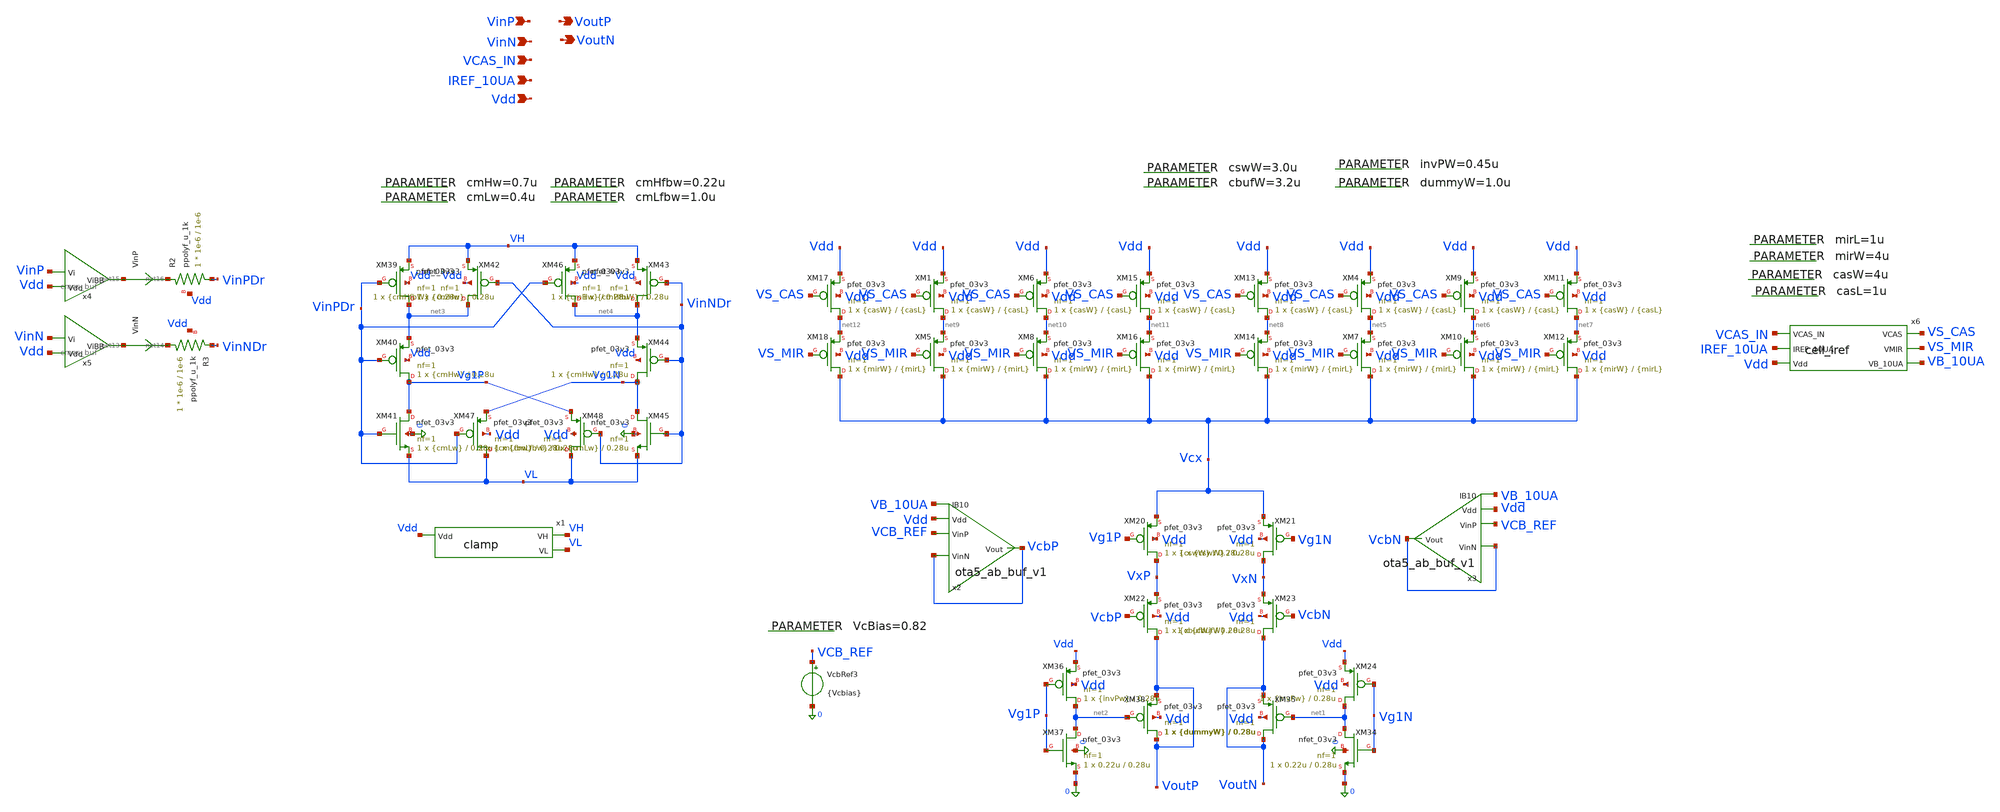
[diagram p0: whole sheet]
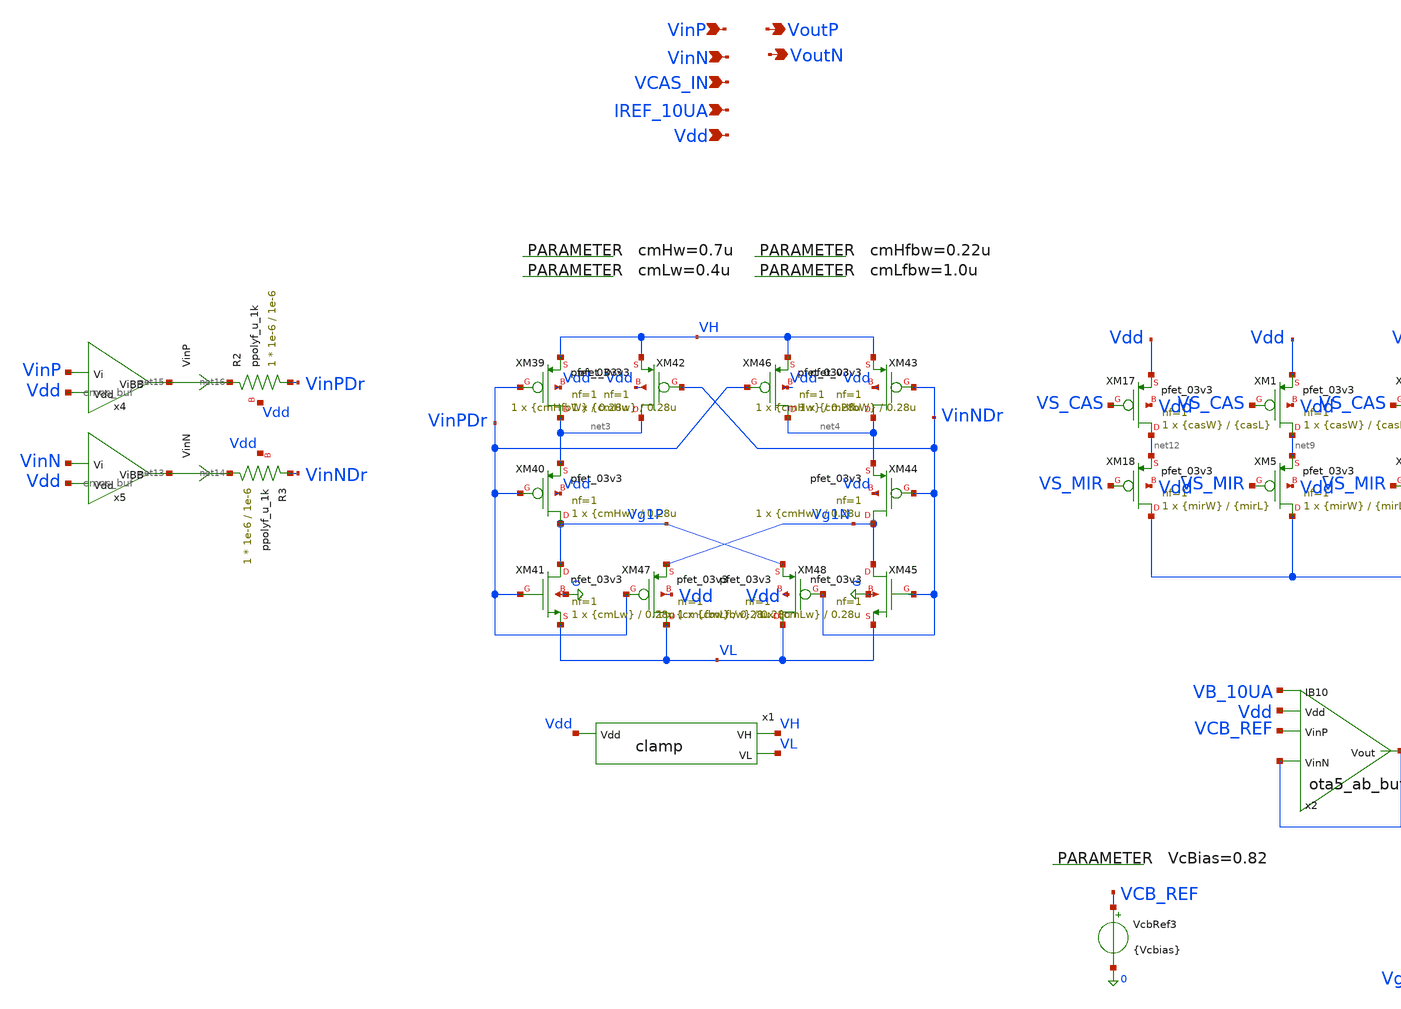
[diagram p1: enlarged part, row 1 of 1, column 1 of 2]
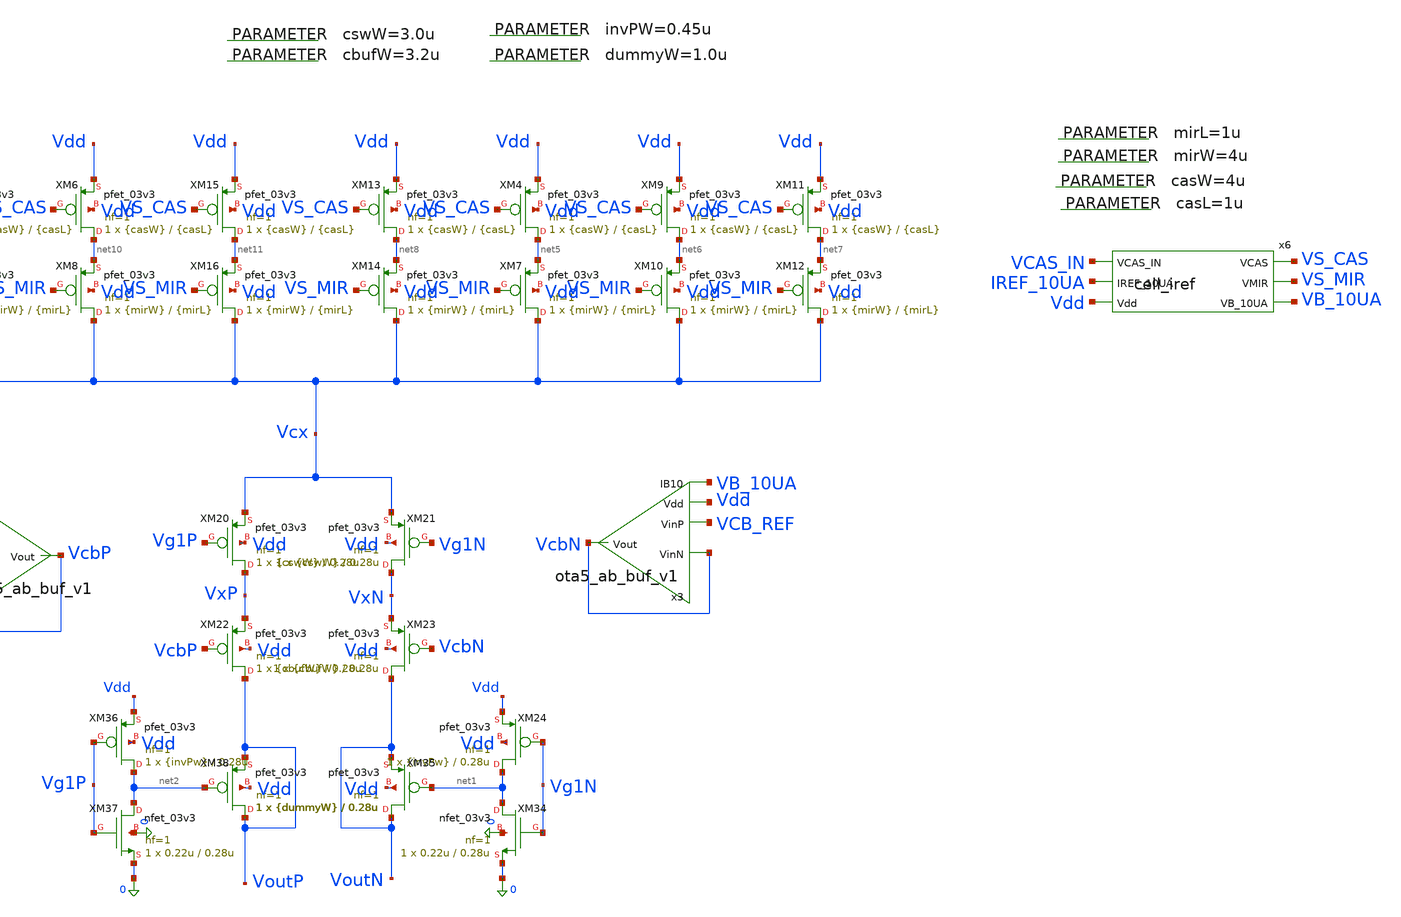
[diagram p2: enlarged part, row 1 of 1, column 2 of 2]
** sch_path: blocks/dac/cellv9/dac_cell_80ua_v9.sch
**.subckt dac_cell_80ua_v9 VoutP VoutN VinP VinN Vdd VCAS_IN IREF_10UA
*.opin VoutP
*.opin VoutN
*.ipin VinP
*.ipin VinN
*.ipin Vdd
*.ipin VCAS_IN
*.ipin IREF_10UA
.param cmLw=0.4u
.param cmHw=0.7u
.param cmLfbw=1.0u
.param cmHfbw=0.22u
XM20 VxP Vg1P Vcx Vdd pfet_03v3 L=0.28u W={cswW} nf=1 ad='int((nf+1)/2) * W/nf * 0.18u' as='int((nf+2)/2) * W/nf * 0.18u'
+ pd='2*int((nf+1)/2) * (W/nf + 0.18u)' ps='2*int((nf+2)/2) * (W/nf + 0.18u)' nrd='0.18u / W' nrs='0.18u / W'
+ sa=0 sb=0 sd=0 m=1
XM21 VxN Vg1N Vcx Vdd pfet_03v3 L=0.28u W={cswW} nf=1 ad='int((nf+1)/2) * W/nf * 0.18u' as='int((nf+2)/2) * W/nf * 0.18u'
+ pd='2*int((nf+1)/2) * (W/nf + 0.18u)' ps='2*int((nf+2)/2) * (W/nf + 0.18u)' nrd='0.18u / W' nrs='0.18u / W'
+ sa=0 sb=0 sd=0 m=1
XM22 VoutP VcbP VxP Vdd pfet_03v3 L=0.28u W={cbufW} nf=1 ad='int((nf+1)/2) * W/nf * 0.18u' as='int((nf+2)/2) * W/nf * 0.18u'
+ pd='2*int((nf+1)/2) * (W/nf + 0.18u)' ps='2*int((nf+2)/2) * (W/nf + 0.18u)' nrd='0.18u / W' nrs='0.18u / W'
+ sa=0 sb=0 sd=0 m=1
XM23 VoutN VcbN VxN Vdd pfet_03v3 L=0.28u W={cbufW} nf=1 ad='int((nf+1)/2) * W/nf * 0.18u' as='int((nf+2)/2) * W/nf * 0.18u'
+ pd='2*int((nf+1)/2) * (W/nf + 0.18u)' ps='2*int((nf+2)/2) * (W/nf + 0.18u)' nrd='0.18u / W' nrs='0.18u / W'
+ sa=0 sb=0 sd=0 m=1
XM24 net1 Vg1N Vdd Vdd pfet_03v3 L=0.28u W={invPw} nf=1 ad='int((nf+1)/2) * W/nf * 0.18u' as='int((nf+2)/2) * W/nf * 0.18u'
+ pd='2*int((nf+1)/2) * (W/nf + 0.18u)' ps='2*int((nf+2)/2) * (W/nf + 0.18u)' nrd='0.18u / W' nrs='0.18u / W'
+ sa=0 sb=0 sd=0 m=1
XM34 net1 Vg1N 0 0 nfet_03v3 L=0.28u W=0.22u nf=1 ad='int((nf+1)/2) * W/nf * 0.18u' as='int((nf+2)/2) * W/nf * 0.18u'
+ pd='2*int((nf+1)/2) * (W/nf + 0.18u)' ps='2*int((nf+2)/2) * (W/nf + 0.18u)' nrd='0.18u / W' nrs='0.18u / W'
+ sa=0 sb=0 sd=0 m=1
XM35 VoutN net1 VoutN Vdd pfet_03v3 L=0.28u W={dummyW} nf=1 ad='int((nf+1)/2) * W/nf * 0.18u' as='int((nf+2)/2) * W/nf * 0.18u'
+ pd='2*int((nf+1)/2) * (W/nf + 0.18u)' ps='2*int((nf+2)/2) * (W/nf + 0.18u)' nrd='0.18u / W' nrs='0.18u / W'
+ sa=0 sb=0 sd=0 m=1
XM36 net2 Vg1P Vdd Vdd pfet_03v3 L=0.28u W={invPw} nf=1 ad='int((nf+1)/2) * W/nf * 0.18u' as='int((nf+2)/2) * W/nf * 0.18u'
+ pd='2*int((nf+1)/2) * (W/nf + 0.18u)' ps='2*int((nf+2)/2) * (W/nf + 0.18u)' nrd='0.18u / W' nrs='0.18u / W'
+ sa=0 sb=0 sd=0 m=1
XM37 net2 Vg1P 0 0 nfet_03v3 L=0.28u W=0.22u nf=1 ad='int((nf+1)/2) * W/nf * 0.18u' as='int((nf+2)/2) * W/nf * 0.18u'
+ pd='2*int((nf+1)/2) * (W/nf + 0.18u)' ps='2*int((nf+2)/2) * (W/nf + 0.18u)' nrd='0.18u / W' nrs='0.18u / W'
+ sa=0 sb=0 sd=0 m=1
XM38 VoutP net2 VoutP Vdd pfet_03v3 L=0.28u W={dummyW} nf=1 ad='int((nf+1)/2) * W/nf * 0.18u' as='int((nf+2)/2) * W/nf * 0.18u'
+ pd='2*int((nf+1)/2) * (W/nf + 0.18u)' ps='2*int((nf+2)/2) * (W/nf + 0.18u)' nrd='0.18u / W' nrs='0.18u / W'
+ sa=0 sb=0 sd=0 m=1
VcbRef3 VCB_REF 0 {Vcbias}
.save i(vcbref3)
.param VcBias=0.82
XM39 net3 VinPDr VH Vdd pfet_03v3 L=0.28u W={cmHw} nf=1 ad='int((nf+1)/2) * W/nf * 0.18u' as='int((nf+2)/2) * W/nf * 0.18u'
+ pd='2*int((nf+1)/2) * (W/nf + 0.18u)' ps='2*int((nf+2)/2) * (W/nf + 0.18u)' nrd='0.18u / W' nrs='0.18u / W'
+ sa=0 sb=0 sd=0 m=1
XM40 Vg1P VinPDr net3 Vdd pfet_03v3 L=0.28u W={cmHw} nf=1 ad='int((nf+1)/2) * W/nf * 0.18u' as='int((nf+2)/2) * W/nf * 0.18u'
+ pd='2*int((nf+1)/2) * (W/nf + 0.18u)' ps='2*int((nf+2)/2) * (W/nf + 0.18u)' nrd='0.18u / W' nrs='0.18u / W'
+ sa=0 sb=0 sd=0 m=1
XM41 Vg1P VinPDr VL 0 nfet_03v3 L=0.28u W={cmLw} nf=1 ad='int((nf+1)/2) * W/nf * 0.18u' as='int((nf+2)/2) * W/nf * 0.18u'
+ pd='2*int((nf+1)/2) * (W/nf + 0.18u)' ps='2*int((nf+2)/2) * (W/nf + 0.18u)' nrd='0.18u / W' nrs='0.18u / W'
+ sa=0 sb=0 sd=0 m=1
XM42 net3 VinNDr VH Vdd pfet_03v3 L=0.28u W={cmHfbW} nf=1 ad='int((nf+1)/2) * W/nf * 0.18u' as='int((nf+2)/2) * W/nf * 0.18u'
+ pd='2*int((nf+1)/2) * (W/nf + 0.18u)' ps='2*int((nf+2)/2) * (W/nf + 0.18u)' nrd='0.18u / W' nrs='0.18u / W'
+ sa=0 sb=0 sd=0 m=1
XM43 net4 VinNDr VH Vdd pfet_03v3 L=0.28u W={cmHw} nf=1 ad='int((nf+1)/2) * W/nf * 0.18u' as='int((nf+2)/2) * W/nf * 0.18u'
+ pd='2*int((nf+1)/2) * (W/nf + 0.18u)' ps='2*int((nf+2)/2) * (W/nf + 0.18u)' nrd='0.18u / W' nrs='0.18u / W'
+ sa=0 sb=0 sd=0 m=1
XM44 Vg1N VinNDr net4 Vdd pfet_03v3 L=0.28u W={cmHw} nf=1 ad='int((nf+1)/2) * W/nf * 0.18u' as='int((nf+2)/2) * W/nf * 0.18u'
+ pd='2*int((nf+1)/2) * (W/nf + 0.18u)' ps='2*int((nf+2)/2) * (W/nf + 0.18u)' nrd='0.18u / W' nrs='0.18u / W'
+ sa=0 sb=0 sd=0 m=1
XM45 Vg1N VinNDr VL 0 nfet_03v3 L=0.28u W={cmLw} nf=1 ad='int((nf+1)/2) * W/nf * 0.18u' as='int((nf+2)/2) * W/nf * 0.18u'
+ pd='2*int((nf+1)/2) * (W/nf + 0.18u)' ps='2*int((nf+2)/2) * (W/nf + 0.18u)' nrd='0.18u / W' nrs='0.18u / W'
+ sa=0 sb=0 sd=0 m=1
XM46 net4 VinPDr VH Vdd pfet_03v3 L=0.28u W={cmHfbW} nf=1 ad='int((nf+1)/2) * W/nf * 0.18u' as='int((nf+2)/2) * W/nf * 0.18u'
+ pd='2*int((nf+1)/2) * (W/nf + 0.18u)' ps='2*int((nf+2)/2) * (W/nf + 0.18u)' nrd='0.18u / W' nrs='0.18u / W'
+ sa=0 sb=0 sd=0 m=1
XM47 VL VinPDr Vg1N Vdd pfet_03v3 L=0.28u W={cmLfbw} nf=1 ad='int((nf+1)/2) * W/nf * 0.18u' as='int((nf+2)/2) * W/nf * 0.18u'
+ pd='2*int((nf+1)/2) * (W/nf + 0.18u)' ps='2*int((nf+2)/2) * (W/nf + 0.18u)' nrd='0.18u / W' nrs='0.18u / W'
+ sa=0 sb=0 sd=0 m=1
XM48 VL VinNDr Vg1P Vdd pfet_03v3 L=0.28u W={cmLfbw} nf=1 ad='int((nf+1)/2) * W/nf * 0.18u' as='int((nf+2)/2) * W/nf * 0.18u'
+ pd='2*int((nf+1)/2) * (W/nf + 0.18u)' ps='2*int((nf+2)/2) * (W/nf + 0.18u)' nrd='0.18u / W' nrs='0.18u / W'
+ sa=0 sb=0 sd=0 m=1
.param dummyW=1.0u
.param invPW=0.45u
.param cswW=3.0u
.param cbufW=3.2u
x1 VH Vdd VL clamp
XM4 net5 VS_CAS Vdd Vdd pfet_03v3 L={casL} W={casW} nf=1 ad='int((nf+1)/2) * W/nf * 0.18u' as='int((nf+2)/2) * W/nf * 0.18u'
+ pd='2*int((nf+1)/2) * (W/nf + 0.18u)' ps='2*int((nf+2)/2) * (W/nf + 0.18u)' nrd='0.18u / W' nrs='0.18u / W'
+ sa=0 sb=0 sd=0 m=1
XM7 Vcx VS_MIR net5 Vdd pfet_03v3 L={mirL} W={mirW} nf=1 ad='int((nf+1)/2) * W/nf * 0.18u' as='int((nf+2)/2) * W/nf * 0.18u'
+ pd='2*int((nf+1)/2) * (W/nf + 0.18u)' ps='2*int((nf+2)/2) * (W/nf + 0.18u)' nrd='0.18u / W' nrs='0.18u / W'
+ sa=0 sb=0 sd=0 m=1
XM9 net6 VS_CAS Vdd Vdd pfet_03v3 L={casL} W={casW} nf=1 ad='int((nf+1)/2) * W/nf * 0.18u' as='int((nf+2)/2) * W/nf * 0.18u'
+ pd='2*int((nf+1)/2) * (W/nf + 0.18u)' ps='2*int((nf+2)/2) * (W/nf + 0.18u)' nrd='0.18u / W' nrs='0.18u / W'
+ sa=0 sb=0 sd=0 m=1
XM10 Vcx VS_MIR net6 Vdd pfet_03v3 L={mirL} W={mirW} nf=1 ad='int((nf+1)/2) * W/nf * 0.18u' as='int((nf+2)/2) * W/nf * 0.18u'
+ pd='2*int((nf+1)/2) * (W/nf + 0.18u)' ps='2*int((nf+2)/2) * (W/nf + 0.18u)' nrd='0.18u / W' nrs='0.18u / W'
+ sa=0 sb=0 sd=0 m=1
XM11 net7 VS_CAS Vdd Vdd pfet_03v3 L={casL} W={casW} nf=1 ad='int((nf+1)/2) * W/nf * 0.18u' as='int((nf+2)/2) * W/nf * 0.18u'
+ pd='2*int((nf+1)/2) * (W/nf + 0.18u)' ps='2*int((nf+2)/2) * (W/nf + 0.18u)' nrd='0.18u / W' nrs='0.18u / W'
+ sa=0 sb=0 sd=0 m=1
XM12 Vcx VS_MIR net7 Vdd pfet_03v3 L={mirL} W={mirW} nf=1 ad='int((nf+1)/2) * W/nf * 0.18u' as='int((nf+2)/2) * W/nf * 0.18u'
+ pd='2*int((nf+1)/2) * (W/nf + 0.18u)' ps='2*int((nf+2)/2) * (W/nf + 0.18u)' nrd='0.18u / W' nrs='0.18u / W'
+ sa=0 sb=0 sd=0 m=1
XM13 net8 VS_CAS Vdd Vdd pfet_03v3 L={casL} W={casW} nf=1 ad='int((nf+1)/2) * W/nf * 0.18u' as='int((nf+2)/2) * W/nf * 0.18u'
+ pd='2*int((nf+1)/2) * (W/nf + 0.18u)' ps='2*int((nf+2)/2) * (W/nf + 0.18u)' nrd='0.18u / W' nrs='0.18u / W'
+ sa=0 sb=0 sd=0 m=1
XM14 Vcx VS_MIR net8 Vdd pfet_03v3 L={mirL} W={mirW} nf=1 ad='int((nf+1)/2) * W/nf * 0.18u' as='int((nf+2)/2) * W/nf * 0.18u'
+ pd='2*int((nf+1)/2) * (W/nf + 0.18u)' ps='2*int((nf+2)/2) * (W/nf + 0.18u)' nrd='0.18u / W' nrs='0.18u / W'
+ sa=0 sb=0 sd=0 m=1
XM1 net9 VS_CAS Vdd Vdd pfet_03v3 L={casL} W={casW} nf=1 ad='int((nf+1)/2) * W/nf * 0.18u' as='int((nf+2)/2) * W/nf * 0.18u'
+ pd='2*int((nf+1)/2) * (W/nf + 0.18u)' ps='2*int((nf+2)/2) * (W/nf + 0.18u)' nrd='0.18u / W' nrs='0.18u / W'
+ sa=0 sb=0 sd=0 m=1
XM5 Vcx VS_MIR net9 Vdd pfet_03v3 L={mirL} W={mirW} nf=1 ad='int((nf+1)/2) * W/nf * 0.18u' as='int((nf+2)/2) * W/nf * 0.18u'
+ pd='2*int((nf+1)/2) * (W/nf + 0.18u)' ps='2*int((nf+2)/2) * (W/nf + 0.18u)' nrd='0.18u / W' nrs='0.18u / W'
+ sa=0 sb=0 sd=0 m=1
XM6 net10 VS_CAS Vdd Vdd pfet_03v3 L={casL} W={casW} nf=1 ad='int((nf+1)/2) * W/nf * 0.18u' as='int((nf+2)/2) * W/nf * 0.18u'
+ pd='2*int((nf+1)/2) * (W/nf + 0.18u)' ps='2*int((nf+2)/2) * (W/nf + 0.18u)' nrd='0.18u / W' nrs='0.18u / W'
+ sa=0 sb=0 sd=0 m=1
XM8 Vcx VS_MIR net10 Vdd pfet_03v3 L={mirL} W={mirW} nf=1 ad='int((nf+1)/2) * W/nf * 0.18u' as='int((nf+2)/2) * W/nf * 0.18u'
+ pd='2*int((nf+1)/2) * (W/nf + 0.18u)' ps='2*int((nf+2)/2) * (W/nf + 0.18u)' nrd='0.18u / W' nrs='0.18u / W'
+ sa=0 sb=0 sd=0 m=1
XM15 net11 VS_CAS Vdd Vdd pfet_03v3 L={casL} W={casW} nf=1 ad='int((nf+1)/2) * W/nf * 0.18u' as='int((nf+2)/2) * W/nf * 0.18u'
+ pd='2*int((nf+1)/2) * (W/nf + 0.18u)' ps='2*int((nf+2)/2) * (W/nf + 0.18u)' nrd='0.18u / W' nrs='0.18u / W'
+ sa=0 sb=0 sd=0 m=1
XM16 Vcx VS_MIR net11 Vdd pfet_03v3 L={mirL} W={mirW} nf=1 ad='int((nf+1)/2) * W/nf * 0.18u' as='int((nf+2)/2) * W/nf * 0.18u'
+ pd='2*int((nf+1)/2) * (W/nf + 0.18u)' ps='2*int((nf+2)/2) * (W/nf + 0.18u)' nrd='0.18u / W' nrs='0.18u / W'
+ sa=0 sb=0 sd=0 m=1
XM17 net12 VS_CAS Vdd Vdd pfet_03v3 L={casL} W={casW} nf=1 ad='int((nf+1)/2) * W/nf * 0.18u' as='int((nf+2)/2) * W/nf * 0.18u'
+ pd='2*int((nf+1)/2) * (W/nf + 0.18u)' ps='2*int((nf+2)/2) * (W/nf + 0.18u)' nrd='0.18u / W' nrs='0.18u / W'
+ sa=0 sb=0 sd=0 m=1
XM18 Vcx VS_MIR net12 Vdd pfet_03v3 L={mirL} W={mirW} nf=1 ad='int((nf+1)/2) * W/nf * 0.18u' as='int((nf+2)/2) * W/nf * 0.18u'
+ pd='2*int((nf+1)/2) * (W/nf + 0.18u)' ps='2*int((nf+2)/2) * (W/nf + 0.18u)' nrd='0.18u / W' nrs='0.18u / W'
+ sa=0 sb=0 sd=0 m=1
x2 Vdd VcbP VCB_REF VcbP VB_10UA ota5_ab_buf_v1
x3 Vdd VcbN VCB_REF VcbN VB_10UA ota5_ab_buf_v1
VinN net13 net14 0
.save i(vinn)
x5 net13 VinN Vdd cmos_buf
VinP net15 net16 0
.save i(vinp)
x4 net15 VinP Vdd cmos_buf
XR3 net14 VinNDr Vdd ppolyf_u_1k r_width=1e-6 r_length=1e-6 m=1
XR2 VinPDr net16 Vdd ppolyf_u_1k r_width=1e-6 r_length=1e-6 m=1
.param casW=4u
.param mirW=4u
.param mirL=1u
.param casL=1u
x6 VCAS_IN VS_CAS VS_MIR IREF_10UA Vdd VB_10UA cell_iref
**.ends

* expanding   symbol:  cellv9/clamp.sym # of pins=3
** sym_path: blocks/dac/cellv9/clamp.sym
** sch_path: blocks/dac/cellv9/clamp.sch
.subckt clamp VH Vdd VL
*.opin VH
*.opin VL
*.ipin Vdd
XM49 VL FB 0 0 nfet_03v3 L=0.28u W=2u nf=1 ad='int((nf+1)/2) * W/nf * 0.18u' as='int((nf+2)/2) * W/nf * 0.18u'
+ pd='2*int((nf+1)/2) * (W/nf + 0.18u)' ps='2*int((nf+2)/2) * (W/nf + 0.18u)' nrd='0.18u / W' nrs='0.18u / W'
+ sa=0 sb=0 sd=0 m=1
XM50 VH FB Vdd Vdd pfet_03v3 L=0.28u W=4u nf=1 ad='int((nf+1)/2) * W/nf * 0.18u' as='int((nf+2)/2) * W/nf * 0.18u'
+ pd='2*int((nf+1)/2) * (W/nf + 0.18u)' ps='2*int((nf+2)/2) * (W/nf + 0.18u)' nrd='0.18u / W' nrs='0.18u / W'
+ sa=0 sb=0 sd=0 m=1
XR3 VL FB Vdd ppolyf_u_1k r_width=1e-6 r_length=1e-6 m=1
XR1 FB VH Vdd ppolyf_u_1k r_width=1e-6 r_length=15e-6 m=1
XC2 Vdd VH cap_mim_2f0_m3m4_noshield c_width=25e-6 c_length=20e-6 m=1
XC1 Vdd VH cap_mim_2f0_m3m4_noshield c_width=10e-6 c_length=5e-6 m=1
XC3 Vdd VH cap_mim_2f0_m3m4_noshield c_width=5e-6 c_length=5e-6 m=1
XC4 VL 0 cap_mim_2f0_m3m4_noshield c_width=25e-6 c_length=20e-6 m=1
XC5 VL 0 cap_mim_2f0_m3m4_noshield c_width=10e-6 c_length=5e-6 m=1
XC6 VL 0 cap_mim_2f0_m3m4_noshield c_width=5e-6 c_length=5e-6 m=1
XC7 Vdd 0 cap_mim_2f0_m3m4_noshield c_width=25e-6 c_length=20e-6 m=1
XC8 FB 0 cap_mim_2f0_m3m4_noshield c_width=10e-6 c_length=5e-6 m=8
.ends


* expanding   symbol:  cellv9/ota5_ab_buf_v1.sym # of pins=5
** sym_path: blocks/dac/cellv9/ota5_ab_buf_v1.sym
** sch_path: blocks/dac/cellv9/ota5_ab_buf_v1.sch
.subckt ota5_ab_buf_v1 Vdd VinN VinP Vout IB10
*.opin Vout
*.ipin VinP
*.ipin VinN
*.ipin Vdd
*.ipin IB10
XM16 VoOTA net2 0 0 nfet_03v3 L=1u W=10u nf=1 ad='int((nf+1)/2) * W/nf * 0.18u' as='int((nf+2)/2) * W/nf * 0.18u'
+ pd='2*int((nf+1)/2) * (W/nf + 0.18u)' ps='2*int((nf+2)/2) * (W/nf + 0.18u)' nrd='0.18u / W' nrs='0.18u / W'
+ sa=0 sb=0 sd=0 m=1
XM18 VoOTA VinN net1 Vdd pfet_03v3 L=1u W=20u nf=1 ad='int((nf+1)/2) * W/nf * 0.18u' as='int((nf+2)/2) * W/nf * 0.18u'
+ pd='2*int((nf+1)/2) * (W/nf + 0.18u)' ps='2*int((nf+2)/2) * (W/nf + 0.18u)' nrd='0.18u / W' nrs='0.18u / W'
+ sa=0 sb=0 sd=0 m=1
XM19 net2 VinP net1 Vdd pfet_03v3 L=1u W=20u nf=1 ad='int((nf+1)/2) * W/nf * 0.18u' as='int((nf+2)/2) * W/nf * 0.18u'
+ pd='2*int((nf+1)/2) * (W/nf + 0.18u)' ps='2*int((nf+2)/2) * (W/nf + 0.18u)' nrd='0.18u / W' nrs='0.18u / W'
+ sa=0 sb=0 sd=0 m=1
XM22 net2 net2 0 0 nfet_03v3 L=1u W=10u nf=1 ad='int((nf+1)/2) * W/nf * 0.18u' as='int((nf+2)/2) * W/nf * 0.18u'
+ pd='2*int((nf+1)/2) * (W/nf + 0.18u)' ps='2*int((nf+2)/2) * (W/nf + 0.18u)' nrd='0.18u / W' nrs='0.18u / W'
+ sa=0 sb=0 sd=0 m=1
XM1 net1 net3 Vdd Vdd pfet_03v3 L=1u W=40u nf=1 ad='int((nf+1)/2) * W/nf * 0.18u' as='int((nf+2)/2) * W/nf * 0.18u'
+ pd='2*int((nf+1)/2) * (W/nf + 0.18u)' ps='2*int((nf+2)/2) * (W/nf + 0.18u)' nrd='0.18u / W' nrs='0.18u / W'
+ sa=0 sb=0 sd=0 m=1
XM2 net3 net3 Vdd Vdd pfet_03v3 L=1u W=40u nf=1 ad='int((nf+1)/2) * W/nf * 0.18u' as='int((nf+2)/2) * W/nf * 0.18u'
+ pd='2*int((nf+1)/2) * (W/nf + 0.18u)' ps='2*int((nf+2)/2) * (W/nf + 0.18u)' nrd='0.18u / W' nrs='0.18u / W'
+ sa=0 sb=0 sd=0 m=1
XM3 VI1b VI1a VI2 Vdd pfet_03v3 L=0.5u W=40u nf=1 ad='int((nf+1)/2) * W/nf * 0.18u' as='int((nf+2)/2) * W/nf * 0.18u'
+ pd='2*int((nf+1)/2) * (W/nf + 0.18u)' ps='2*int((nf+2)/2) * (W/nf + 0.18u)' nrd='0.18u / W' nrs='0.18u / W'
+ sa=0 sb=0 sd=0 m=1
XM4 VI2 VoOTA Vout 0 nfet_03v3 L=0.5u W=80u nf=1 ad='int((nf+1)/2) * W/nf * 0.18u' as='int((nf+2)/2) * W/nf * 0.18u'
+ pd='2*int((nf+1)/2) * (W/nf + 0.18u)' ps='2*int((nf+2)/2) * (W/nf + 0.18u)' nrd='0.18u / W' nrs='0.18u / W'
+ sa=0 sb=0 sd=0 m=1
XM5 Vout VI2 Vdd Vdd pfet_03v3 L=1u W=80u nf=1 ad='int((nf+1)/2) * W/nf * 0.18u' as='int((nf+2)/2) * W/nf * 0.18u'
+ pd='2*int((nf+1)/2) * (W/nf + 0.18u)' ps='2*int((nf+2)/2) * (W/nf + 0.18u)' nrd='0.18u / W' nrs='0.18u / W'
+ sa=0 sb=0 sd=0 m=1
XM6 Vout VI1b 0 0 nfet_03v3 L=0.5u W=40u nf=1 ad='int((nf+1)/2) * W/nf * 0.18u' as='int((nf+2)/2) * W/nf * 0.18u'
+ pd='2*int((nf+1)/2) * (W/nf + 0.18u)' ps='2*int((nf+2)/2) * (W/nf + 0.18u)' nrd='0.18u / W' nrs='0.18u / W'
+ sa=0 sb=0 sd=0 m=1
XM7 VI1a VI1a VI0 Vdd pfet_03v3 L=0.5u W=40u nf=1 ad='int((nf+1)/2) * W/nf * 0.18u' as='int((nf+2)/2) * W/nf * 0.18u'
+ pd='2*int((nf+1)/2) * (W/nf + 0.18u)' ps='2*int((nf+2)/2) * (W/nf + 0.18u)' nrd='0.18u / W' nrs='0.18u / W'
+ sa=0 sb=0 sd=0 m=1
XM8 VI1a VI0 Vdd Vdd pfet_03v3 L=1u W=80u nf=1 ad='int((nf+1)/2) * W/nf * 0.18u' as='int((nf+2)/2) * W/nf * 0.18u'
+ pd='2*int((nf+1)/2) * (W/nf + 0.18u)' ps='2*int((nf+2)/2) * (W/nf + 0.18u)' nrd='0.18u / W' nrs='0.18u / W'
+ sa=0 sb=0 sd=0 m=1
XM11 VI0 net4 Vdd Vdd pfet_03v3 L=0.5u W=80u nf=1 ad='int((nf+1)/2) * W/nf * 0.18u' as='int((nf+2)/2) * W/nf * 0.18u'
+ pd='2*int((nf+1)/2) * (W/nf + 0.18u)' ps='2*int((nf+2)/2) * (W/nf + 0.18u)' nrd='0.18u / W' nrs='0.18u / W'
+ sa=0 sb=0 sd=0 m=1
XM12 net4 net4 Vdd Vdd pfet_03v3 L=0.5u W=80u nf=1 ad='int((nf+1)/2) * W/nf * 0.18u' as='int((nf+2)/2) * W/nf * 0.18u'
+ pd='2*int((nf+1)/2) * (W/nf + 0.18u)' ps='2*int((nf+2)/2) * (W/nf + 0.18u)' nrd='0.18u / W' nrs='0.18u / W'
+ sa=0 sb=0 sd=0 m=1
XM9 VI2 net4 Vdd Vdd pfet_03v3 L=0.5u W=80u nf=1 ad='int((nf+1)/2) * W/nf * 0.18u' as='int((nf+2)/2) * W/nf * 0.18u'
+ pd='2*int((nf+1)/2) * (W/nf + 0.18u)' ps='2*int((nf+2)/2) * (W/nf + 0.18u)' nrd='0.18u / W' nrs='0.18u / W'
+ sa=0 sb=0 sd=0 m=1
XM10 net5 net5 Vdd Vdd pfet_03v3 L=0.5u W=40u nf=1 ad='int((nf+1)/2) * W/nf * 0.18u' as='int((nf+2)/2) * W/nf * 0.18u'
+ pd='2*int((nf+1)/2) * (W/nf + 0.18u)' ps='2*int((nf+2)/2) * (W/nf + 0.18u)' nrd='0.18u / W' nrs='0.18u / W'
+ sa=0 sb=0 sd=0 m=1
XM15 IB30Ref net5 Vdd Vdd pfet_03v3 L=0.5u W=40u nf=1 ad='int((nf+1)/2) * W/nf * 0.18u' as='int((nf+2)/2) * W/nf * 0.18u'
+ pd='2*int((nf+1)/2) * (W/nf + 0.18u)' ps='2*int((nf+2)/2) * (W/nf + 0.18u)' nrd='0.18u / W' nrs='0.18u / W'
+ sa=0 sb=0 sd=0 m=1
XM17 IB30Ref IB30Ref 0 0 nfet_03v3 L=0.5u W=40u nf=1 ad='int((nf+1)/2) * W/nf * 0.18u' as='int((nf+2)/2) * W/nf * 0.18u'
+ pd='2*int((nf+1)/2) * (W/nf + 0.18u)' ps='2*int((nf+2)/2) * (W/nf + 0.18u)' nrd='0.18u / W' nrs='0.18u / W'
+ sa=0 sb=0 sd=0 m=1
XM20 VI1a IB30Ref 0 0 nfet_03v3 L=0.5u W=40u nf=1 ad='int((nf+1)/2) * W/nf * 0.18u' as='int((nf+2)/2) * W/nf * 0.18u'
+ pd='2*int((nf+1)/2) * (W/nf + 0.18u)' ps='2*int((nf+2)/2) * (W/nf + 0.18u)' nrd='0.18u / W' nrs='0.18u / W'
+ sa=0 sb=0 sd=0 m=1
XM21 VI1b IB30Ref 0 0 nfet_03v3 L=0.5u W=40u nf=1 ad='int((nf+1)/2) * W/nf * 0.18u' as='int((nf+2)/2) * W/nf * 0.18u'
+ pd='2*int((nf+1)/2) * (W/nf + 0.18u)' ps='2*int((nf+2)/2) * (W/nf + 0.18u)' nrd='0.18u / W' nrs='0.18u / W'
+ sa=0 sb=0 sd=0 m=2
XM13 net4 IB30Ref 0 0 nfet_03v3 L=0.5u W=40u nf=1 ad='int((nf+1)/2) * W/nf * 0.18u' as='int((nf+2)/2) * W/nf * 0.18u'
+ pd='2*int((nf+1)/2) * (W/nf + 0.18u)' ps='2*int((nf+2)/2) * (W/nf + 0.18u)' nrd='0.18u / W' nrs='0.18u / W'
+ sa=0 sb=0 sd=0 m=2
XM30 net3 IB10 0 0 nfet_03v3 L=1u W=8u nf=1 ad='int((nf+1)/2) * W/nf * 0.18u' as='int((nf+2)/2) * W/nf * 0.18u'
+ pd='2*int((nf+1)/2) * (W/nf + 0.18u)' ps='2*int((nf+2)/2) * (W/nf + 0.18u)' nrd='0.18u / W' nrs='0.18u / W'
+ sa=0 sb=0 sd=0 m=2
XM14 net5 IB10 0 0 nfet_03v3 L=1u W=8u nf=1 ad='int((nf+1)/2) * W/nf * 0.18u' as='int((nf+2)/2) * W/nf * 0.18u'
+ pd='2*int((nf+1)/2) * (W/nf + 0.18u)' ps='2*int((nf+2)/2) * (W/nf + 0.18u)' nrd='0.18u / W' nrs='0.18u / W'
+ sa=0 sb=0 sd=0 m=3
.ends


* expanding   symbol:  common/cmos_buf.sym # of pins=3
** sym_path: blocks/dac/common/cmos_buf.sym
** sch_path: blocks/dac/common/cmos_buf.sch
.subckt cmos_buf ViBB Vi Vdd
*.ipin Vi
*.opin ViBB
*.ipin Vdd
XM49 ViB Vi 0 0 nfet_03v3 L=0.28u W=0.5u nf=1 ad='int((nf+1)/2) * W/nf * 0.18u' as='int((nf+2)/2) * W/nf * 0.18u'
+ pd='2*int((nf+1)/2) * (W/nf + 0.18u)' ps='2*int((nf+2)/2) * (W/nf + 0.18u)' nrd='0.18u / W' nrs='0.18u / W'
+ sa=0 sb=0 sd=0 m=1
XM50 ViB Vi Vdd Vdd pfet_03v3 L=0.28u W=1u nf=1 ad='int((nf+1)/2) * W/nf * 0.18u' as='int((nf+2)/2) * W/nf * 0.18u'
+ pd='2*int((nf+1)/2) * (W/nf + 0.18u)' ps='2*int((nf+2)/2) * (W/nf + 0.18u)' nrd='0.18u / W' nrs='0.18u / W'
+ sa=0 sb=0 sd=0 m=1
XM1 ViBB ViB 0 0 nfet_03v3 L=0.28u W=0.5u nf=1 ad='int((nf+1)/2) * W/nf * 0.18u' as='int((nf+2)/2) * W/nf * 0.18u'
+ pd='2*int((nf+1)/2) * (W/nf + 0.18u)' ps='2*int((nf+2)/2) * (W/nf + 0.18u)' nrd='0.18u / W' nrs='0.18u / W'
+ sa=0 sb=0 sd=0 m=1
XM2 ViBB ViB Vdd Vdd pfet_03v3 L=0.28u W=1u nf=1 ad='int((nf+1)/2) * W/nf * 0.18u' as='int((nf+2)/2) * W/nf * 0.18u'
+ pd='2*int((nf+1)/2) * (W/nf + 0.18u)' ps='2*int((nf+2)/2) * (W/nf + 0.18u)' nrd='0.18u / W' nrs='0.18u / W'
+ sa=0 sb=0 sd=0 m=1
.ends


* expanding   symbol:  cellv9/cell_iref.sym # of pins=6
** sym_path: blocks/dac/cellv9/cell_iref.sym
** sch_path: blocks/dac/cellv9/cell_iref.sch
.subckt cell_iref VCAS_IN VCAS VMIR IREF_10UA Vdd VB_10UA
*.opin VMIR
*.opin VCAS
*.ipin Vdd
*.ipin VCAS_IN
*.ipin IREF_10UA
*.opin VB_10UA
XM1 IREF_10UA IREF_10UA net1 Vdd pfet_03v3 L={mirL} W={mirW} nf=1 ad='int((nf+1)/2) * W/nf * 0.18u' as='int((nf+2)/2) * W/nf * 0.18u'
+ pd='2*int((nf+1)/2) * (W/nf + 0.18u)' ps='2*int((nf+2)/2) * (W/nf + 0.18u)' nrd='0.18u / W' nrs='0.18u / W'
+ sa=0 sb=0 sd=0 m=1
XM49 net1 VCAS Vdd Vdd pfet_03v3 L={casL} W={casW} nf=1 ad='int((nf+1)/2) * W/nf * 0.18u' as='int((nf+2)/2) * W/nf * 0.18u'
+ pd='2*int((nf+1)/2) * (W/nf + 0.18u)' ps='2*int((nf+2)/2) * (W/nf + 0.18u)' nrd='0.18u / W' nrs='0.18u / W'
+ sa=0 sb=0 sd=0 m=1
XM8 VB_10UA VMIR net2 Vdd pfet_03v3 L={mirL} W={mirW} nf=1 ad='int((nf+1)/2) * W/nf * 0.18u' as='int((nf+2)/2) * W/nf * 0.18u'
+ pd='2*int((nf+1)/2) * (W/nf + 0.18u)' ps='2*int((nf+2)/2) * (W/nf + 0.18u)' nrd='0.18u / W' nrs='0.18u / W'
+ sa=0 sb=0 sd=0 m=1
XM25 net2 VCAS Vdd Vdd pfet_03v3 L={casL} W={casW} nf=1 ad='int((nf+1)/2) * W/nf * 0.18u' as='int((nf+2)/2) * W/nf * 0.18u'
+ pd='2*int((nf+1)/2) * (W/nf + 0.18u)' ps='2*int((nf+2)/2) * (W/nf + 0.18u)' nrd='0.18u / W' nrs='0.18u / W'
+ sa=0 sb=0 sd=0 m=1
XM26 VB_10UA VB_10UA 0 0 nfet_03v3 L=1u W=8u nf=1 ad='int((nf+1)/2) * W/nf * 0.18u' as='int((nf+2)/2) * W/nf * 0.18u'
+ pd='2*int((nf+1)/2) * (W/nf + 0.18u)' ps='2*int((nf+2)/2) * (W/nf + 0.18u)' nrd='0.18u / W' nrs='0.18u / W'
+ sa=0 sb=0 sd=0 m=1
XR4 VCAS_IN VCAS Vdd ppolyf_u_1k r_width=2e-6 r_length=10e-6 m=1
XC1 VCAS 0 cap_mim_2f0_m3m4_noshield c_width=5e-6 c_length=5e-6 m=1
.param casW=4u
.param mirW=4u
.param mirL=1u
.param casL=1u
XR1 IREF_10UA VMIR Vdd ppolyf_u_1k r_width=2e-6 r_length=10e-6 m=1
XC2 VMIR 0 cap_mim_2f0_m3m4_noshield c_width=5e-6 c_length=5e-6 m=1
.ends

.end
